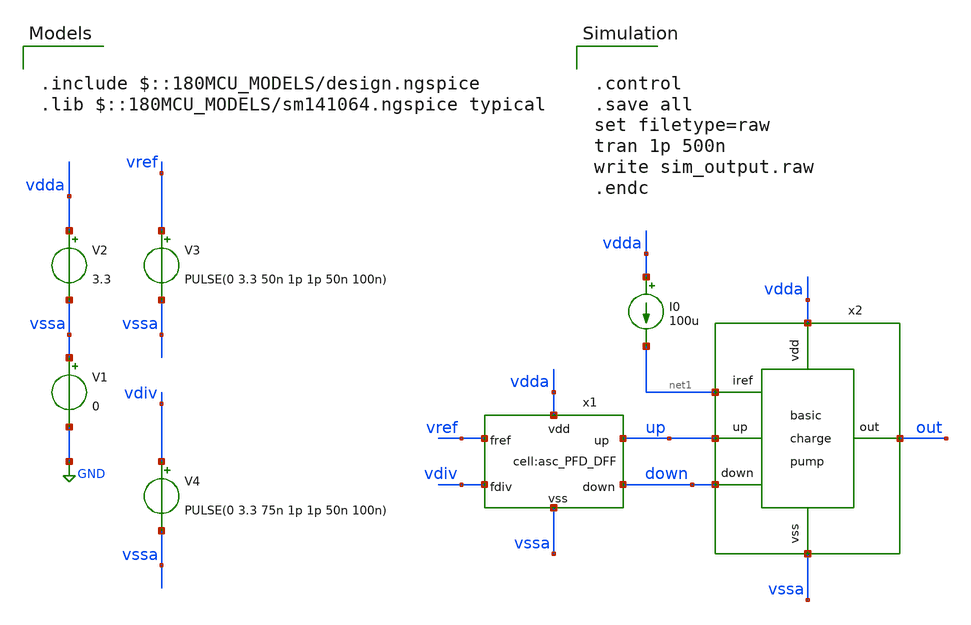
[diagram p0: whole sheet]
** sch_path: designs/libs/tb_analog/tb_asc_basic_pump/tb_asc_basic_pump.sch
**.subckt tb_asc_basic_pump
V1 vssa GND 0
V2 vdda vssa 3.3
V3 vref vssa PULSE(0 3.3 50n 1p 1p 50n 100n)
V4 vdiv vssa PULSE(0 3.3 75n 1p 1p 50n 100n)
x1 vdda vssa down up vref vdiv asc_PFD_DFF
x2 vdda out vssa down up net1 asc_basic_pump
I0 vdda net1 100u
**** begin user architecture code

.include $::180MCU_MODELS/design.ngspice
.lib $::180MCU_MODELS/sm141064.ngspice typical



.control
.save all
set filetype=raw
tran 1p 500n
write sim_output.raw
.endc


**** end user architecture code
**.ends
.GLOBAL GND
.end
